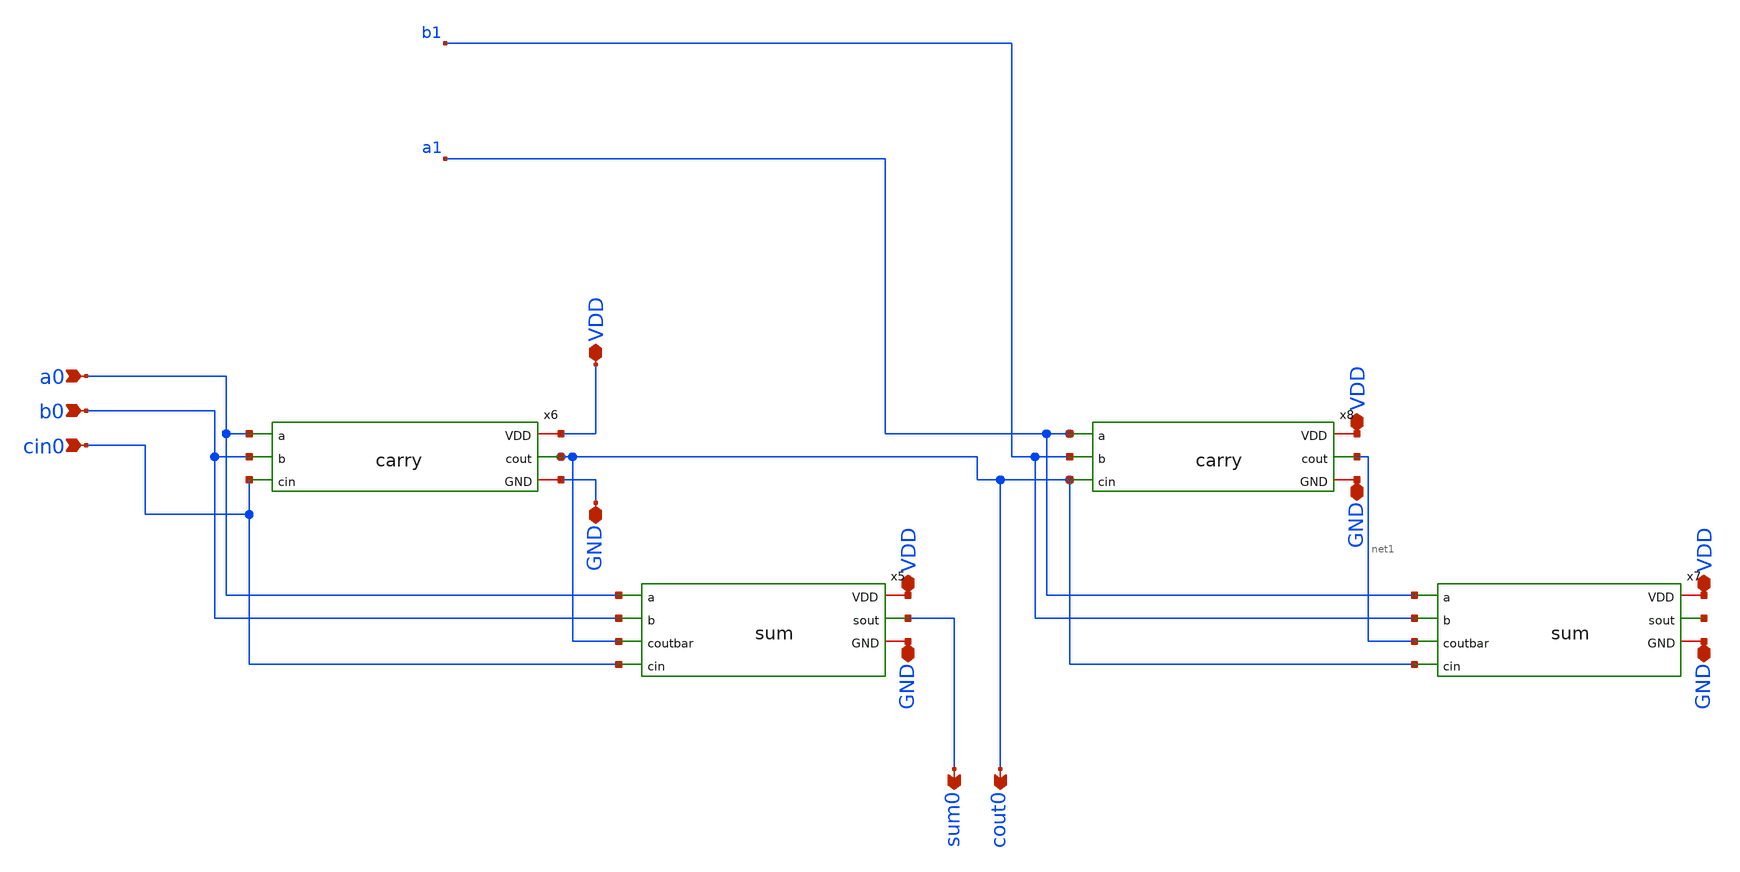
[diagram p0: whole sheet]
** sch_path: assignments/assignment8/rca8.sch
**.subckt rca8 GND VDD GND GND GND VDD VDD a0 sum0 VDD b0 cin0 cout0
*.iopin GND
*.iopin VDD
*.iopin GND
*.iopin GND
*.iopin GND
*.iopin VDD
*.iopin VDD
*.ipin a0
*.opin sum0
*.iopin VDD
*.ipin b0
*.ipin cin0
*.opin cout0
x5 VDD a0 b0 cout0 cin0 sum0 GND sum
x6 VDD a0 b0 cin0 cout0 GND carry
x7 VDD a1 b1 net1 cout0 net2 GND sum
x8 VDD a1 b1 cout0 net1 GND carry
**.ends
.end
